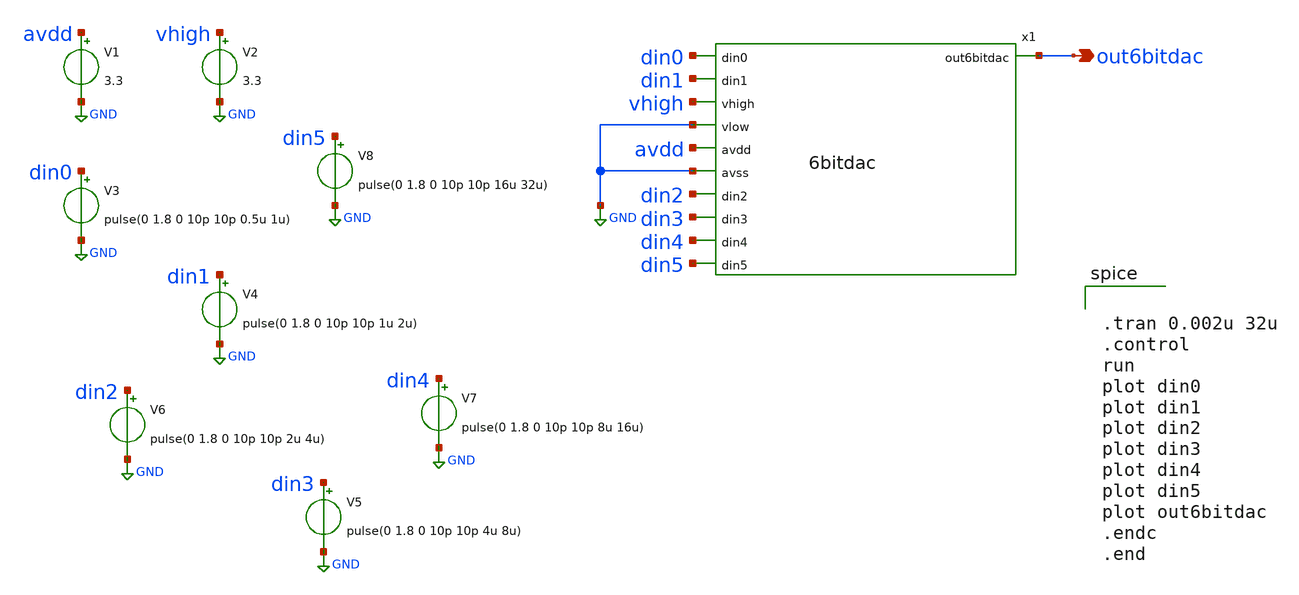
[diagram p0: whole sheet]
** sch_path: xschem/tb_6bitdac.sch
**.subckt tb_6bitdac out6bitdac
*.opin out6bitdac
x1 out6bitdac din0 din1 vhigh GND avdd GND din2 din3 din4 din5 6bitdac
V1 avdd GND 3.3
V2 vhigh GND 3.3
V3 din0 GND pulse(0 1.8 0 10p 10p 0.5u 1u)
V4 din1 GND pulse(0 1.8 0 10p 10p 1u 2u)
V6 din2 GND pulse(0 1.8 0 10p 10p 2u 4u)
V5 din3 GND pulse(0 1.8 0 10p 10p 4u 8u)
V7 din4 GND pulse(0 1.8 0 10p 10p 8u 16u)
V8 din5 GND pulse(0 1.8 0 10p 10p 16u 32u)
**** begin user architecture code

** opencircuitdesign pdks install
.lib $::SKYWATER_MODELS/sky130.lib.spice tt




.tran 0.002u 32u
.control
run
plot din0
plot din1
plot din2
plot din3
plot din4
plot din5
plot out6bitdac
.endc
.end

**** end user architecture code
**.ends
.GLOBAL GND
.end
